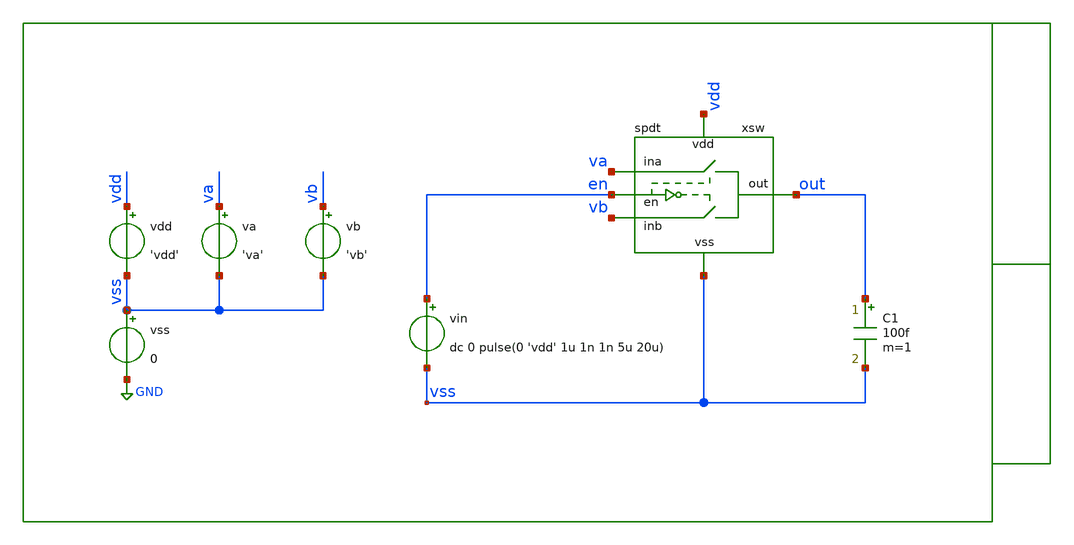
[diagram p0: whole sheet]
** sch_path: xschem/tb/spdt/spdt/tr_spdt.sch
**.subckt tr_spdt
vdd vdd vss 'vdd'
vss vss GND 0
vin en vss dc 0 pulse(0 'vdd' 1u 1n 1n 5u 20u)
C1 out vss 100f m=1
xsw out en vdd vb vss va spdt
va va vss 'va'
vb vb vss 'vb'
**** begin user architecture code

* Control

.param vdd = 3.3
.temp 27

.param va = 0.5
.param vb = 2.5

.control
save all

tran 1n 10u
gnuplot p1 out

.endc
.end


 * Model Corners

.include $::CORNERS/ngspice/tt.spice
*.include $::CORNERS/ngspice/ff.spice
*.include $::CORNERS/ngspice/ss.spice
*.include $::CORNERS/ngspice/sf.spice
*.include $::CORNERS/ngspice/fs.spice

**** end user architecture code
**.ends

* expanding   symbol:  sch/spdt/spdt/spdt.sym # of pins=6
** sym_path: xschem/sch/spdt/spdt/spdt.sym
** sch_path: xschem/sch/spdt/spdt/spdt.sch
.subckt spdt out en vdd inb vss ina
*.ipin en
*.iopin vss
*.iopin vdd
*.iopin ina
*.iopin out
*.iopin inb
XMI1 enb_buf en vss vss nfet_06v0 L=1u W=4u nf=1 ad='int((nf+1)/2) * W/nf * 0.18u' as='int((nf+2)/2) * W/nf * 0.18u'
+ pd='2*int((nf+1)/2) * (W/nf + 0.18u)' ps='2*int((nf+2)/2) * (W/nf + 0.18u)' nrd='0.18u / W' nrs='0.18u / W'
+ sa=0 sb=0 sd=0 m=1 par=1
XMI2 en_buf enb_buf vss vss nfet_06v0 L=1u W=4u nf=1 ad='int((nf+1)/2) * W/nf * 0.18u' as='int((nf+2)/2) * W/nf * 0.18u'
+ pd='2*int((nf+1)/2) * (W/nf + 0.18u)' ps='2*int((nf+2)/2) * (W/nf + 0.18u)' nrd='0.18u / W' nrs='0.18u / W'
+ sa=0 sb=0 sd=0 m=1 par=1
XMI3 enb_buf en vdd vdd pfet_06v0 L=1u W=8u nf=1 ad='int((nf+1)/2) * W/nf * 0.18u' as='int((nf+2)/2) * W/nf * 0.18u'
+ pd='2*int((nf+1)/2) * (W/nf + 0.18u)' ps='2*int((nf+2)/2) * (W/nf + 0.18u)' nrd='0.18u / W' nrs='0.18u / W'
+ sa=0 sb=0 sd=0 m=1 par=1
XMI4 en_buf enb_buf vdd vdd pfet_06v0 L=1u W=8u nf=1 ad='int((nf+1)/2) * W/nf * 0.18u' as='int((nf+2)/2) * W/nf * 0.18u'
+ pd='2*int((nf+1)/2) * (W/nf + 0.18u)' ps='2*int((nf+2)/2) * (W/nf + 0.18u)' nrd='0.18u / W' nrs='0.18u / W'
+ sa=0 sb=0 sd=0 m=1 par=1
XM2 inb en_buf out vdd pfet_06v0 L=1u W=64u nf=8 ad='int((nf+1)/2) * W/nf * 0.18u' as='int((nf+2)/2) * W/nf * 0.18u'
+ pd='2*int((nf+1)/2) * (W/nf + 0.18u)' ps='2*int((nf+2)/2) * (W/nf + 0.18u)' nrd='0.18u / W' nrs='0.18u / W'
+ sa=0 sb=0 sd=0 m=1 par=1
XM1 inb enb_buf out vss nfet_06v0 L=1u W=32u nf=4 ad='int((nf+1)/2) * W/nf * 0.18u' as='int((nf+2)/2) * W/nf * 0.18u'
+ pd='2*int((nf+1)/2) * (W/nf + 0.18u)' ps='2*int((nf+2)/2) * (W/nf + 0.18u)' nrd='0.18u / W' nrs='0.18u / W'
+ sa=0 sb=0 sd=0 m=1 par=1
XM3 ina en_buf out vss nfet_06v0 L=1u W=32u nf=4 ad='int((nf+1)/2) * W/nf * 0.18u' as='int((nf+2)/2) * W/nf * 0.18u'
+ pd='2*int((nf+1)/2) * (W/nf + 0.18u)' ps='2*int((nf+2)/2) * (W/nf + 0.18u)' nrd='0.18u / W' nrs='0.18u / W'
+ sa=0 sb=0 sd=0 m=1 par=1
XM4 ina enb_buf out vdd pfet_06v0 L=1u W=64u nf=8 ad='int((nf+1)/2) * W/nf * 0.18u' as='int((nf+2)/2) * W/nf * 0.18u'
+ pd='2*int((nf+1)/2) * (W/nf + 0.18u)' ps='2*int((nf+2)/2) * (W/nf + 0.18u)' nrd='0.18u / W' nrs='0.18u / W'
+ sa=0 sb=0 sd=0 m=1 par=1
.ends

.GLOBAL GND
.end
